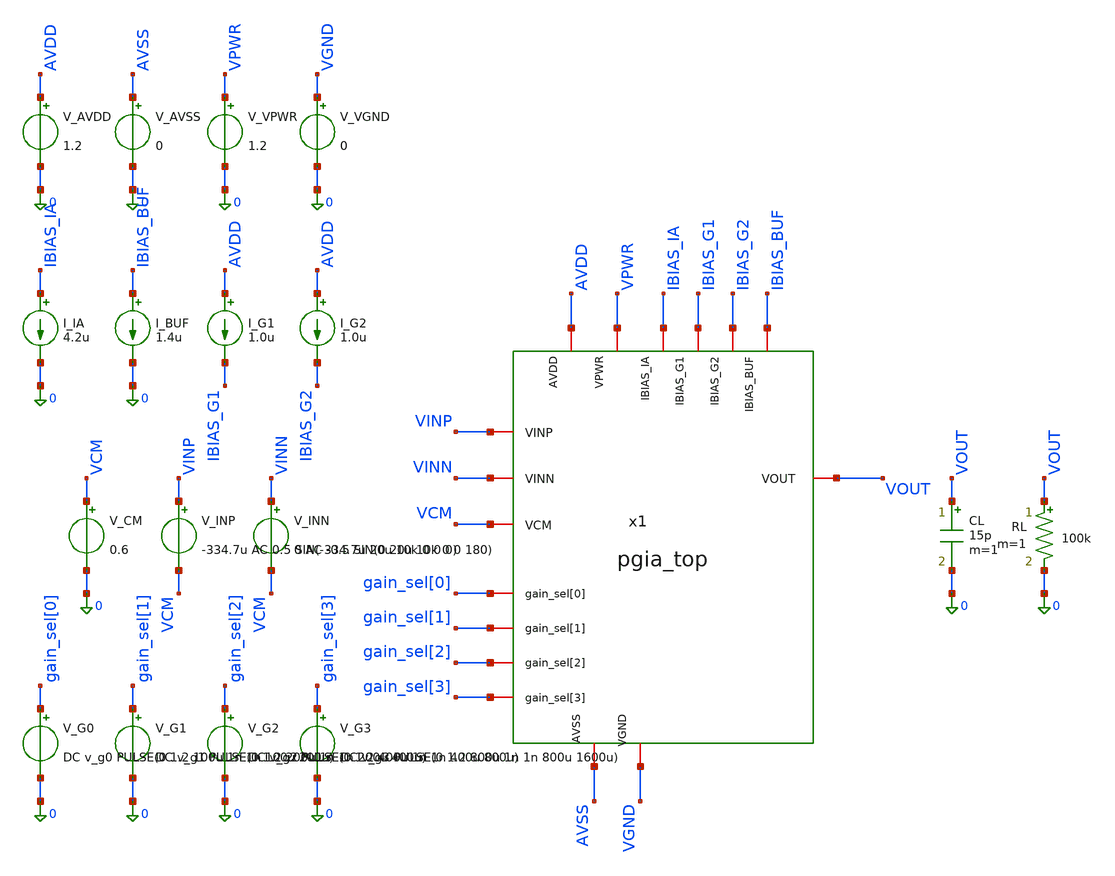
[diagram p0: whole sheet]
** sch_path: xschem/pgia_top/tb_pgia_top.sch
**.subckt tb_pgia_top
x1 VINP VINN VCM gain_sel[0] gain_sel[1] gain_sel[2] gain_sel[3] VOUT AVDD VPWR IBIAS_IA IBIAS_G1
+ IBIAS_G2 IBIAS_BUF AVSS VGND pgia_top
V_AVDD AVDD 0 1.2
V_AVSS AVSS 0 0
V_VPWR VPWR 0 1.2
V_VGND VGND 0 0
I_IA IBIAS_IA 0 4.2u
I_BUF IBIAS_BUF 0 1.4u
I_G1 AVDD IBIAS_G1 1.0u
I_G2 AVDD IBIAS_G2 1.0u
V_CM VCM 0 0.6
V_INP VINP VCM -334.7u AC 0.5 SIN(-334.7u 20u 10k 0 0 0)
V_INN VINN VCM 0 AC -0.5 SIN(0 20u 10k 0 0 180)
V_G0 gain_sel[0] 0 DC v_g0 PULSE(0 1.2 100u 1n 1n 100u 200u)
V_G1 gain_sel[1] 0 DC v_g1 PULSE(0 1.2 200u 1n 1n 200u 400u)
V_G2 gain_sel[2] 0 DC v_g2 PULSE(0 1.2 400u 1n 1n 400u 800u)
V_G3 gain_sel[3] 0 DC v_g3 PULSE(0 1.2 800u 1n 1n 800u 1600u)
CL VOUT 0 15p m=1
RL VOUT 0 100k m=1
**** begin user architecture code


.lib /foss/pdks/ihp-sg13cmos5l/libs.tech/ngspice/models/cornerMOSlv.lib mos_tt
.lib /foss/pdks/ihp-sg13cmos5l/libs.tech/ngspice/models/cornerRES.lib res_typ
.lib /foss/pdks/ihp-sg13cmos5l/libs.tech/ngspice/models/cornerCAP.lib cap_typ
.include /foss/pdks/ihp-sg13cmos5l/libs.ref/sg13cmos5l_stdcell/spice/sg13cmos5l_stdcell.spice

.param temp=27
.param lbias=0.15u wbias=0.15u
.param m6=1 m7=4 m8=8
.param linpair=3u winpair=20u
.param lload=5u wload=10u
.param lcs=3u wcs=20u
.param Cc=2p
.param v_g0=0 v_g1=0 v_g2=0 v_g3=0

.save v_inp#branch v_inn#branch v(VOUT) v(VINP) v(VINN) v(VCM) v(x1.v_ia) v(x1.v_stage1) v(x1.v_stage2) v_avdd#branch v_vpwr#branch




.control
  save all v(VOUT) v(x1.v_ia) v(x1.v_stage1) v(x1.v_stage2) v_inp#branch v_inn#branch
  echo ==========================================================================
  echo === TOP-LEVEL PGIA CO-SIMULATION BATTERY (MILESTONES 3, 4, 5) ===
  echo ==========================================================================

  * 1. DC Operating Point Verification
  echo
  echo --- Phase A: DC Operating Point Audit ---
  op
  let v_ia_dc     = v(x1.v_ia)
  let v_st1_dc    = v(x1.v_stage1)
  let v_st2_dc    = v(x1.v_stage2)
  let v_out_dc    = v(VOUT)
  let v_diff_dc   = v(VINP) - v(VINN)
  let i_avdd_dc   = -v_avdd#branch
  let i_vpwr_dc   = -v_vpwr#branch
  let p_tot_uW    = (i_avdd_dc + i_vpwr_dc) * 1.2 * 1e6

  echo Target Common-Mode: 0.600 V
  echo V(VINP) - V(VINN) = $&v_diff_dc V
  echo V(v_ia)           = $&v_ia_dc V
  echo V(v_stage1)       = $&v_st1_dc V
  echo V(v_stage2)       = $&v_st2_dc V
  echo V(VOUT)           = $&v_out_dc V
  echo Total Static DC Power = $&p_tot_uW uW (Spec Target: under 500 uW)

  * 2. Small-Signal AC Gain Sweeps Across All 11 Valid Gain Steps (0 to 10)
  echo
  echo --- Phase B: Small-Signal AC Frequency Response (11 Steps) ---

  * Step 0: 0000 (Target: 18.06 dB / 8x)
  alterparam v_g0=0
  alterparam v_g1=0
  alterparam v_g2=0
  alterparam v_g3=0
  reset
  op
  let v_out_dc0 = v(VOUT)
  set vdc0 = $&v_out_dc0
  let vos0_val = ($vdc0 - 0.6) * 1000
  set vos0 = $&vos0_val
  ac dec 10 10 100Meg
  let gain0 = db(v(VOUT))
  let g0_1k = gain0[20]
  echo Step 0  (0000): Gain @ 1kHz = $&g0_1k dB, V_OUT_dc = $vdc0 V, V_OS_out = $vos0 mV

  * Step 1: 0001 (Target: 24.08 dB / 16x)
  alterparam v_g0=1.2
  alterparam v_g1=0
  alterparam v_g2=0
  alterparam v_g3=0
  reset
  op
  let v_out_dc1 = v(VOUT)
  set vdc1 = $&v_out_dc1
  let vos1_val = ($vdc1 - 0.6) * 1000
  set vos1 = $&vos1_val
  ac dec 10 10 100Meg
  let gain1 = db(v(VOUT))
  let g1_1k = gain1[20]
  echo Step 1  (0001): Gain @ 1kHz = $&g1_1k dB, V_OUT_dc = $vdc1 V, V_OS_out = $vos1 mV

  * Step 2: 0010 (Target: 30.10 dB / 32x)
  alterparam v_g0=0
  alterparam v_g1=1.2
  alterparam v_g2=0
  alterparam v_g3=0
  reset
  op
  let v_out_dc2 = v(VOUT)
  set vdc2 = $&v_out_dc2
  let vos2_val = ($vdc2 - 0.6) * 1000
  set vos2 = $&vos2_val
  ac dec 10 10 100Meg
  let gain2 = db(v(VOUT))
  let g2_1k = gain2[20]
  echo Step 2  (0010): Gain @ 1kHz = $&g2_1k dB, V_OUT_dc = $vdc2 V, V_OS_out = $vos2 mV

  * Step 3: 0011 (Target: 36.12 dB / 64x)
  alterparam v_g0=1.2
  alterparam v_g1=1.2
  alterparam v_g2=0
  alterparam v_g3=0
  reset
  op
  let v_out_dc3 = v(VOUT)
  set vdc3 = $&v_out_dc3
  let vos3_val = ($vdc3 - 0.6) * 1000
  set vos3 = $&vos3_val
  ac dec 10 10 100Meg
  let gain3 = db(v(VOUT))
  let g3_1k = gain3[20]
  echo Step 3  (0011): Gain @ 1kHz = $&g3_1k dB, V_OUT_dc = $vdc3 V, V_OS_out = $vos3 mV

  * Step 4: 0100 (Target: 42.14 dB / 128x)
  alterparam v_g0=0
  alterparam v_g1=0
  alterparam v_g2=1.2
  alterparam v_g3=0
  reset
  op
  let v_out_dc4 = v(VOUT)
  set vdc4 = $&v_out_dc4
  let vos4_val = ($vdc4 - 0.6) * 1000
  set vos4 = $&vos4_val
  ac dec 10 10 100Meg
  let gain4 = db(v(VOUT))
  let g4_1k = gain4[20]
  echo Step 4  (0100): Gain @ 1kHz = $&g4_1k dB, V_OUT_dc = $vdc4 V, V_OS_out = $vos4 mV

  * Step 5: 0101 (Target: 48.16 dB / 256x)
  alterparam v_g0=1.2
  alterparam v_g1=0
  alterparam v_g2=1.2
  alterparam v_g3=0
  reset
  op
  let v_out_dc5 = v(VOUT)
  set vdc5 = $&v_out_dc5
  let vos5_val = ($vdc5 - 0.6) * 1000
  set vos5 = $&vos5_val
  ac dec 10 10 100Meg
  let gain5 = db(v(VOUT))
  let g5_1k = gain5[20]
  echo Step 5  (0101): Gain @ 1kHz = $&g5_1k dB, V_OUT_dc = $vdc5 V, V_OS_out = $vos5 mV

  * Step 6: 0110 (Target: 54.18 dB / 512x)
  alterparam v_g0=0
  alterparam v_g1=1.2
  alterparam v_g2=1.2
  alterparam v_g3=0
  reset
  op
  let v_out_dc6 = v(VOUT)
  set vdc6 = $&v_out_dc6
  let vos6_val = ($vdc6 - 0.6) * 1000
  set vos6 = $&vos6_val
  ac dec 10 10 100Meg
  let gain6 = db(v(VOUT))
  let g6_1k = gain6[20]
  echo Step 6  (0110): Gain @ 1kHz = $&g6_1k dB, V_OUT_dc = $vdc6 V, V_OS_out = $vos6 mV

  * Step 7: 0111 (Target: 60.20 dB / 1024x)
  alterparam v_g0=1.2
  alterparam v_g1=1.2
  alterparam v_g2=1.2
  alterparam v_g3=0
  reset
  op
  let v_out_dc7 = v(VOUT)
  set vdc7 = $&v_out_dc7
  let vos7_val = ($vdc7 - 0.6) * 1000
  set vos7 = $&vos7_val
  ac dec 10 10 100Meg
  let gain7 = db(v(VOUT))
  let g7_1k = gain7[20]
  echo Step 7  (0111): Gain @ 1kHz = $&g7_1k dB, V_OUT_dc = $vdc7 V, V_OS_out = $vos7 mV

  * Step 8: 1000 (Target: 66.22 dB / 2048x)
  alterparam v_g0=0
  alterparam v_g1=0
  alterparam v_g2=0
  alterparam v_g3=1.2
  reset
  op
  let v_out_dc8 = v(VOUT)
  set vdc8 = $&v_out_dc8
  let vos8_val = ($vdc8 - 0.6) * 1000
  set vos8 = $&vos8_val
  ac dec 10 10 100Meg
  let gain8 = db(v(VOUT))
  let g8_1k = gain8[20]
  echo Step 8  (1000): Gain @ 1kHz = $&g8_1k dB, V_OUT_dc = $vdc8 V, V_OS_out = $vos8 mV

  * Step 9: 1001 (Target: 72.24 dB / 4096x)
  alterparam v_g0=1.2
  alterparam v_g1=0
  alterparam v_g2=0
  alterparam v_g3=1.2
  reset
  op
  let v_out_dc9 = v(VOUT)
  set vdc9 = $&v_out_dc9
  let vos9_val = ($vdc9 - 0.6) * 1000
  set vos9 = $&vos9_val
  ac dec 10 10 100Meg
  let gain9 = db(v(VOUT))
  let g9_1k = gain9[20]
  echo Step 9  (1001): Gain @ 1kHz = $&g9_1k dB, V_OUT_dc = $vdc9 V, V_OS_out = $vos9 mV

  * Step 10: 1010 (Target: 78.26 dB / 8192x)
  alterparam v_g0=0
  alterparam v_g1=1.2
  alterparam v_g2=0
  alterparam v_g3=1.2
  reset
  op
  let v_out_dc10 = v(VOUT)
  set vdc10 = $&v_out_dc10
  let vos10_val = ($vdc10 - 0.6) * 1000
  set vos10 = $&vos10_val
  ac dec 10 10 100Meg
  let gain10 = db(v(VOUT))
  let g10_1k = gain10[20]
  echo Step 10 (1010): Gain @ 1kHz = $&g10_1k dB, V_OUT_dc = $vdc10 V, V_OS_out = $vos10 mV

  * Step 11: 1011 (Out-of-range Clamp Target)
  alterparam v_g0=1.2
  alterparam v_g1=1.2
  alterparam v_g2=0
  alterparam v_g3=1.2
  reset
  op
  let v_out_dc11 = v(VOUT)
  set vdc11 = $&v_out_dc11
  let vos11_val = ($vdc11 - 0.6) * 1000
  set vos11 = $&vos11_val
  ac dec 10 10 100Meg
  let gain11 = db(v(VOUT))
  let g11_1k = gain11[20]
  echo Step 11 (1011): Gain @ 1kHz = $&g11_1k dB, V_OUT_dc = $vdc11 V, V_OS_out = $vos11 mV
+ (Expected Clamp to Step 0)

  * 3. Dynamic Transient Co-Simulation Across All 16 States (0 to 15)
  echo
  echo --- Phase C: Dynamic Transient Stepping (16 States x 100us) ---
  tran 1u 1.6m
  meas tran vpp_st0  pp  v(VOUT) from=50u to=90u
  meas tran vdc_st0  avg v(VOUT) from=50u to=90u
  let vos_st0 = (vdc_st0 - 0.6) * 1000

  meas tran vpp_st1  pp  v(VOUT) from=150u to=190u
  meas tran vdc_st1  avg v(VOUT) from=150u to=190u
  let vos_st1 = (vdc_st1 - 0.6) * 1000

  meas tran vpp_st2  pp  v(VOUT) from=250u to=290u
  meas tran vdc_st2  avg v(VOUT) from=250u to=290u
  let vos_st2 = (vdc_st2 - 0.6) * 1000

  meas tran vpp_st3  pp  v(VOUT) from=350u to=390u
  meas tran vdc_st3  avg v(VOUT) from=350u to=390u
  let vos_st3 = (vdc_st3 - 0.6) * 1000

  meas tran vpp_st4  pp  v(VOUT) from=450u to=490u
  meas tran vdc_st4  avg v(VOUT) from=450u to=490u
  let vos_st4 = (vdc_st4 - 0.6) * 1000

  meas tran vpp_st5  pp  v(VOUT) from=550u to=590u
  meas tran vdc_st5  avg v(VOUT) from=550u to=590u
  let vos_st5 = (vdc_st5 - 0.6) * 1000

  meas tran vpp_st6  pp  v(VOUT) from=650u to=690u
  meas tran vdc_st6  avg v(VOUT) from=650u to=690u
  let vos_st6 = (vdc_st6 - 0.6) * 1000

  meas tran vpp_st7  pp  v(VOUT) from=750u to=790u
  meas tran vdc_st7  avg v(VOUT) from=750u to=790u
  let vos_st7 = (vdc_st7 - 0.6) * 1000

  meas tran vpp_st8  pp  v(VOUT) from=850u to=890u
  meas tran vdc_st8  avg v(VOUT) from=850u to=890u
  let vos_st8 = (vdc_st8 - 0.6) * 1000

  meas tran vpp_st9  pp  v(VOUT) from=950u to=990u
  meas tran vdc_st9  avg v(VOUT) from=950u to=990u
  let vos_st9 = (vdc_st9 - 0.6) * 1000

  meas tran vpp_st10 pp  v(VOUT) from=1050u to=1090u
  meas tran vdc_st10 avg v(VOUT) from=1050u to=1090u
  let vos_st10 = (vdc_st10 - 0.6) * 1000

  meas tran vpp_st11 pp  v(VOUT) from=1150u to=1190u
  meas tran vdc_st11 avg v(VOUT) from=1150u to=1190u
  let vos_st11 = (vdc_st11 - 0.6) * 1000

  meas tran vpp_st12 pp  v(VOUT) from=1250u to=1290u
  meas tran vdc_st12 avg v(VOUT) from=1250u to=1290u
  let vos_st12 = (vdc_st12 - 0.6) * 1000

  meas tran vpp_st15 pp  v(VOUT) from=1550u to=1590u
  meas tran vdc_st15 avg v(VOUT) from=1550u to=1590u
  let vos_st15 = (vdc_st15 - 0.6) * 1000

  echo
  echo Transient Output Peak-to-Peak and DC Offset:
  echo State 0  (0000): $&vpp_st0 Vpp, V_OUT_dc = $&vdc_st0 V, V_OS_out = $&vos_st0 mV
  echo State 1  (0001): $&vpp_st1 Vpp, V_OUT_dc = $&vdc_st1 V, V_OS_out = $&vos_st1 mV
  echo State 2  (0010): $&vpp_st2 Vpp, V_OUT_dc = $&vdc_st2 V, V_OS_out = $&vos_st2 mV
  echo State 3  (0011): $&vpp_st3 Vpp, V_OUT_dc = $&vdc_st3 V, V_OS_out = $&vos_st3 mV
  echo State 4  (0100): $&vpp_st4 Vpp, V_OUT_dc = $&vdc_st4 V, V_OS_out = $&vos_st4 mV
  echo State 5  (0101): $&vpp_st5 Vpp, V_OUT_dc = $&vdc_st5 V, V_OS_out = $&vos_st5 mV
  echo State 6  (0110): $&vpp_st6 Vpp, V_OUT_dc = $&vdc_st6 V, V_OS_out = $&vos_st6 mV
  echo State 7  (0111): $&vpp_st7 Vpp, V_OUT_dc = $&vdc_st7 V, V_OS_out = $&vos_st7 mV
  echo State 8  (1000): $&vpp_st8 Vpp, V_OUT_dc = $&vdc_st8 V, V_OS_out = $&vos_st8 mV
  echo State 9  (1001): $&vpp_st9 Vpp, V_OUT_dc = $&vdc_st9 V, V_OS_out = $&vos_st9 mV
  echo State 10 (1010): $&vpp_st10 Vpp, V_OUT_dc = $&vdc_st10 V, V_OS_out = $&vos_st10 mV
  echo State 11 (1011): $&vpp_st11 Vpp (Clamped), V_OUT_dc = $&vdc_st11 V, V_OS_out = $&vos_st11 mV
  echo State 12 (1100): $&vpp_st12 Vpp (Clamped), V_OUT_dc = $&vdc_st12 V, V_OS_out = $&vos_st12 mV
  echo State 15 (1111): $&vpp_st15 Vpp (Clamped), V_OUT_dc = $&vdc_st15 V, V_OS_out = $&vos_st15 mV

  * 4. Pseudo-Resistor Input Resistance & Non-linear R-V Characterization
  echo
  echo --- Phase D: Pseudo-Resistor Characterization (Small-Signal AC & Narrow DC) ---

  * Method 1: Ultra-low Frequency Small-Signal AC (1 mHz)
  alterparam v_g0=0
  alterparam v_g1=0
  alterparam v_g2=0
  alterparam v_g3=0
  reset
  alter @v_inp[acmag] = 1.0
  alter @v_inn[acmag] = 1.0
  save all v_inp#branch v_inn#branch
  ac dec 10 0.001 1k
  let r_ac_p_giga = (1.0 / (abs(v_inp#branch[0]) + 1e-25)) / 1e9
  let r_ac_n_giga = (1.0 / (abs(v_inn#branch[0]) + 1e-25)) / 1e9
  let r_ac_p_mega = r_ac_p_giga * 1000.0
  let r_ac_n_mega = r_ac_n_giga * 1000.0

  echo Method 1 (Small-Signal AC @ 1mHz):
  echo   R_pseudo_AC (VINP - VCM) = $&r_ac_p_mega MOhms ($&r_ac_p_giga GOhms)
  echo   R_pseudo_AC (VINN - VCM) = $&r_ac_n_mega MOhms ($&r_ac_n_giga GOhms)

  * Method 2: Narrow DC Sweep (+/-50mV around VCM) & Dynamic Derivative R = dV / dI
  save all v_inp#branch v_inn#branch
  dc v_inp -50m 50m 0.5m
  let i_branch = -v_inp#branch
  let g_dyn = deriv(i_branch)
  let r_dyn = 1.0 / (g_dyn + 1e-25)
  meas dc r_peak_dc find r_dyn at=0
  meas dc r_m20_dc  find r_dyn at=-20m
  meas dc r_p20_dc  find r_dyn at=20m
  meas dc r_m50_dc  find r_dyn at=-50m
  meas dc r_p50_dc  find r_dyn at=50m

  let r_peak_giga = r_peak_dc / 1e9
  let r_m20_giga  = r_m20_dc / 1e9
  let r_p20_giga  = r_p20_dc / 1e9
  let r_m50_giga  = r_m50_dc / 1e9
  let r_p50_giga  = r_p50_dc / 1e9

  let r_peak_mega = r_peak_dc / 1e6
  let r_m20_mega  = r_m20_dc / 1e6
  let r_p20_mega  = r_p20_dc / 1e6
  let r_m50_mega  = r_m50_dc / 1e6
  let r_p50_mega  = r_p50_dc / 1e6

  echo Method 2 (Narrow DC Sweep Derivative):
  echo   R_pseudo_DC Peak @ 0.000V (Quiescent) = $&r_peak_mega MOhms ($&r_peak_giga GOhms)
  echo   R_pseudo_DC @ -20mV (-20mV vs VCM)    = $&r_m20_mega MOhms ($&r_m20_giga GOhms)
  echo   R_pseudo_DC @ +20mV (+20mV vs VCM)    = $&r_p20_mega MOhms ($&r_p20_giga GOhms)
  echo   R_pseudo_DC @ -50mV (-50mV vs VCM)    = $&r_m50_mega MOhms ($&r_m50_giga GOhms)
  echo   R_pseudo_DC @ +50mV (+50mV vs VCM)    = $&r_p50_mega MOhms ($&r_p50_giga GOhms)

  echo ==========================================================================
  echo === SIMULATION COMPLETE ===
  echo ==========================================================================
.endc


**** end user architecture code
**.ends
.end
